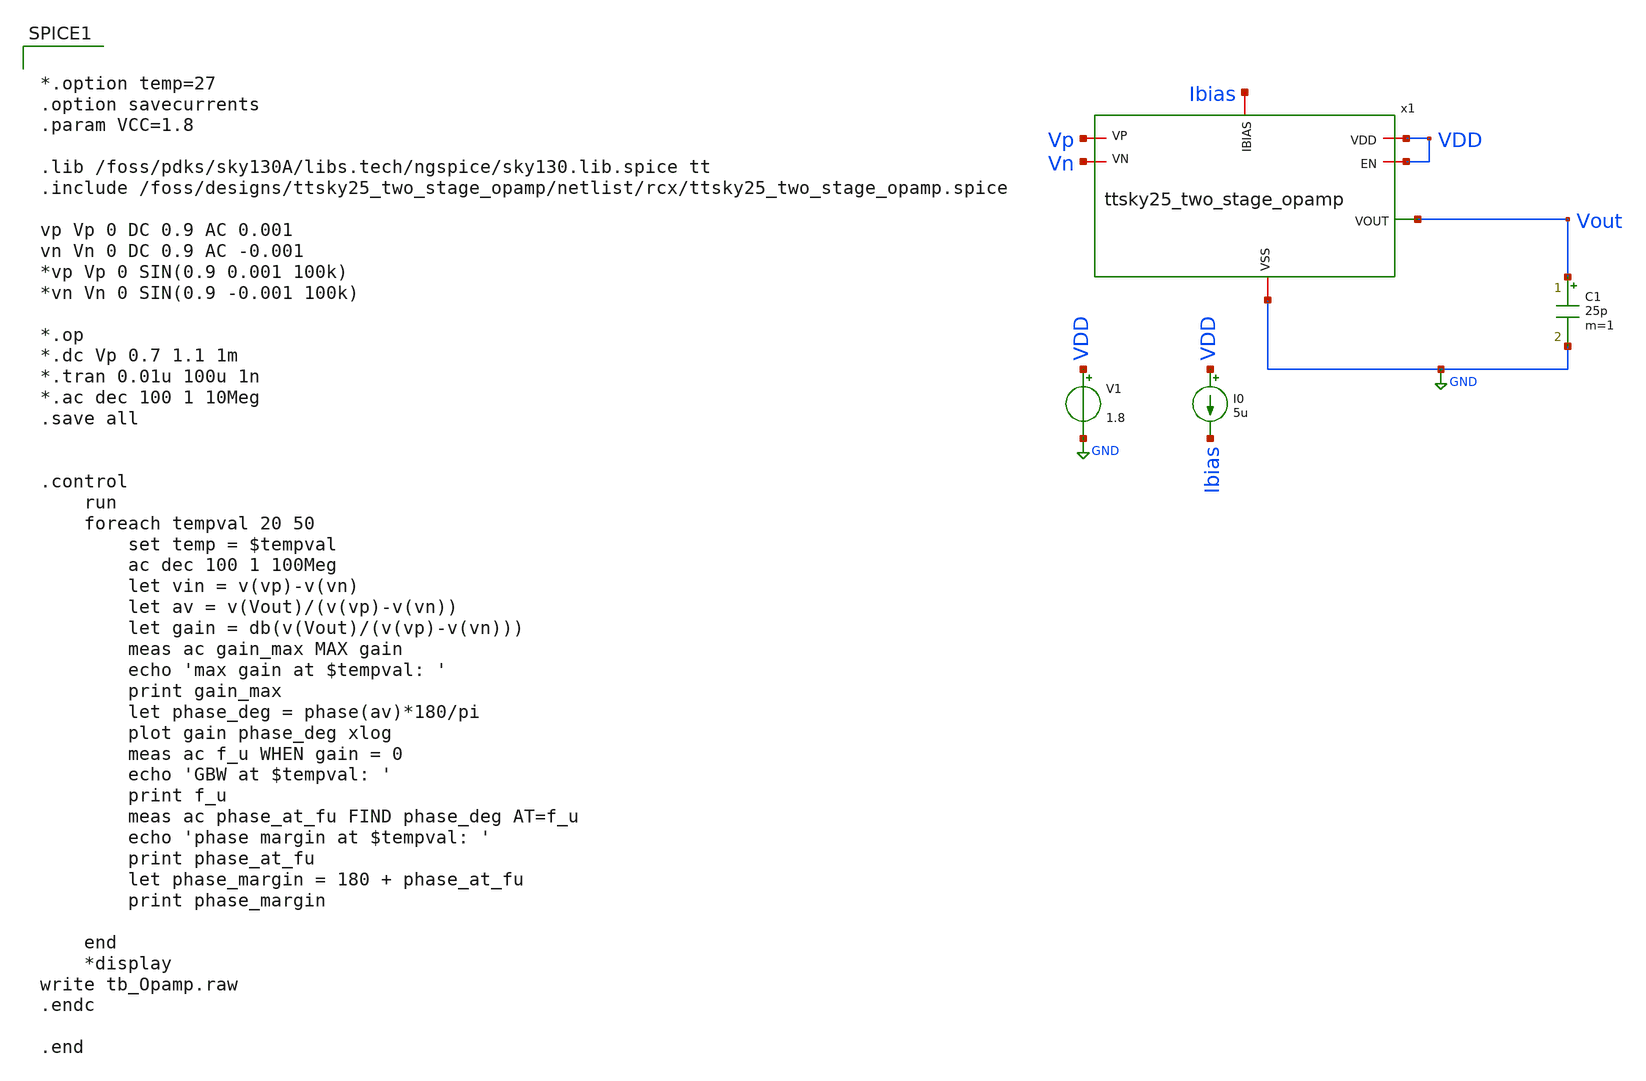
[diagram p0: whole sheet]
** sch_path: xschem/post-layout/testbenches/tb_Opamp.sch
**.subckt tb_Opamp
V1 VDD GND 1.8
C1 Vout GND 25p m=1
I0 VDD Ibias 5u
x1 VDD Ibias Vout Vn Vp VDD GND ttsky25_two_stage_opamp
**** begin user architecture code


*.option temp=27
.option savecurrents
.param VCC=1.8

.lib /foss/pdks/sky130A/libs.tech/ngspice/sky130.lib.spice tt
.include /foss/designs/ttsky25_two_stage_opamp/netlist/rcx/ttsky25_two_stage_opamp.spice

vp Vp 0 DC 0.9 AC 0.001
vn Vn 0 DC 0.9 AC -0.001
*vp Vp 0 SIN(0.9 0.001 100k)
*vn Vn 0 SIN(0.9 -0.001 100k)

*.op
*.dc Vp 0.7 1.1 1m
*.tran 0.01u 100u 1n
*.ac dec 100 1 10Meg
.save all


.control
	run
	foreach tempval 20 50
		set temp = $tempval
		ac dec 100 1 100Meg
		let vin = v(vp)-v(vn)
		let av = v(Vout)/(v(vp)-v(vn))
		let gain = db(v(Vout)/(v(vp)-v(vn)))
		meas ac gain_max MAX gain
		echo 'max gain at $tempval: '
		print gain_max
		let phase_deg = phase(av)*180/pi
		plot gain phase_deg xlog
		meas ac f_u WHEN gain = 0
		echo 'GBW at $tempval: '
		print f_u
		meas ac phase_at_fu FIND phase_deg AT=f_u
		echo 'phase margin at $tempval: '
		print phase_at_fu
		let phase_margin = 180 + phase_at_fu
		print phase_margin

	end
	*display
write tb_Opamp.raw
.endc

.end


**** end user architecture code
**.ends

* expanding   symbol:  ttsky25_two_stage_opamp.sym # of pins=7
** sym_path: xschem/ttsky25_two_stage_opamp.sym
** sch_path: xschem/ttsky25_two_stage_opamp.sch
.subckt ttsky25_two_stage_opamp VDD IBIAS VOUT VN VP EN VSS
*.iopin VSS
*.iopin VDD
*.iopin IBIAS
*.opin VOUT
*.iopin EN
*.iopin VN
*.iopin VP
XC2 net1 VOUT sky130_fd_pr__cap_mim_m3_1 W=25.5 L=25.5 MF=1 m=1
XM5 net2 net2 net2 VSS sky130_fd_pr__nfet_01v8_lvt L=1 W=7 nf=1 ad='int((1 + 1)/2) * 7 / 1 * 0.29' as='int((1 + 2)/2) * 7 / 1 * 0.29'
+ pd='2*int((1 + 1)/2) * (7 / 1 + 0.29)' ps='2*int((1 + 2)/2) * (7 / 1 + 0.29)' nrd='0.29 / 7 ' nrs='0.29 / 7 '
+ sa=0 sb=0 sd=0 mult=1 m=1
XM6 IBIAS EN net2 VSS sky130_fd_pr__nfet_01v8_lvt L=1 W=7 nf=1 ad='int((1 + 1)/2) * 7 / 1 * 0.29' as='int((1 + 2)/2) * 7 / 1 * 0.29'
+ pd='2*int((1 + 1)/2) * (7 / 1 + 0.29)' ps='2*int((1 + 2)/2) * (7 / 1 + 0.29)' nrd='0.29 / 7 ' nrs='0.29 / 7 '
+ sa=0 sb=0 sd=0 mult=1 m=1
XM8 IBIAS IBIAS IBIAS VSS sky130_fd_pr__nfet_01v8_lvt L=1 W=7 nf=1 ad='int((1 + 1)/2) * 7 / 1 * 0.29'
+ as='int((1 + 2)/2) * 7 / 1 * 0.29' pd='2*int((1 + 1)/2) * (7 / 1 + 0.29)' ps='2*int((1 + 2)/2) * (7 / 1 + 0.29)'
+ nrd='0.29 / 7 ' nrs='0.29 / 7 ' sa=0 sb=0 sd=0 mult=1 m=1
XM9 Vz Vz Vz VSS sky130_fd_pr__nfet_01v8_lvt L=1 W=7 nf=1 ad='int((1 + 1)/2) * 7 / 1 * 0.29' as='int((1 + 2)/2) * 7 / 1 * 0.29'
+ pd='2*int((1 + 1)/2) * (7 / 1 + 0.29)' ps='2*int((1 + 2)/2) * (7 / 1 + 0.29)' nrd='0.29 / 7 ' nrs='0.29 / 7 '
+ sa=0 sb=0 sd=0 mult=1 m=1
XM10 Vz EN net3 VSS sky130_fd_pr__nfet_01v8_lvt L=1 W=7 nf=1 ad='int((1 + 1)/2) * 7 / 1 * 0.29' as='int((1 + 2)/2) * 7 / 1 * 0.29'
+ pd='2*int((1 + 1)/2) * (7 / 1 + 0.29)' ps='2*int((1 + 2)/2) * (7 / 1 + 0.29)' nrd='0.29 / 7 ' nrs='0.29 / 7 '
+ sa=0 sb=0 sd=0 mult=1 m=1
XM11 net3 net3 net3 VSS sky130_fd_pr__nfet_01v8_lvt L=1 W=7 nf=1 ad='int((1 + 1)/2) * 7 / 1 * 0.29' as='int((1 + 2)/2) * 7 / 1 * 0.29'
+ pd='2*int((1 + 1)/2) * (7 / 1 + 0.29)' ps='2*int((1 + 2)/2) * (7 / 1 + 0.29)' nrd='0.29 / 7 ' nrs='0.29 / 7 '
+ sa=0 sb=0 sd=0 mult=1 m=1
XM13 VOUT EN net4 VSS sky130_fd_pr__nfet_01v8_lvt L=1 W=7 nf=1 ad='int((1 + 1)/2) * 7 / 1 * 0.29' as='int((1 + 2)/2) * 7 / 1 * 0.29'
+ pd='2*int((1 + 1)/2) * (7 / 1 + 0.29)' ps='2*int((1 + 2)/2) * (7 / 1 + 0.29)' nrd='0.29 / 7 ' nrs='0.29 / 7 '
+ sa=0 sb=0 sd=0 mult=1 m=1
XM14 VOUT VOUT VOUT VSS sky130_fd_pr__nfet_01v8_lvt L=1 W=7 nf=1 ad='int((1 + 1)/2) * 7 / 1 * 0.29' as='int((1 + 2)/2) * 7 / 1 * 0.29'
+ pd='2*int((1 + 1)/2) * (7 / 1 + 0.29)' ps='2*int((1 + 2)/2) * (7 / 1 + 0.29)' nrd='0.29 / 7 ' nrs='0.29 / 7 '
+ sa=0 sb=0 sd=0 mult=1 m=1
XM15 net4 net4 net4 VSS sky130_fd_pr__nfet_01v8_lvt L=1 W=7 nf=1 ad='int((1 + 1)/2) * 7 / 1 * 0.29' as='int((1 + 2)/2) * 7 / 1 * 0.29'
+ pd='2*int((1 + 1)/2) * (7 / 1 + 0.29)' ps='2*int((1 + 2)/2) * (7 / 1 + 0.29)' nrd='0.29 / 7 ' nrs='0.29 / 7 '
+ sa=0 sb=0 sd=0 mult=1 m=1
XM16 net2 net2 VSS VSS sky130_fd_pr__nfet_01v8_lvt L=1 W=3 nf=1 ad='int((1 + 1)/2) * 3 / 1 * 0.29' as='int((1 + 2)/2) * 3 / 1 * 0.29'
+ pd='2*int((1 + 1)/2) * (3 / 1 + 0.29)' ps='2*int((1 + 2)/2) * (3 / 1 + 0.29)' nrd='0.29 / 3 ' nrs='0.29 / 3 '
+ sa=0 sb=0 sd=0 mult=1 m=1
XM17 net2 net2 VSS VSS sky130_fd_pr__nfet_01v8_lvt L=1 W=3 nf=1 ad='int((1 + 1)/2) * 3 / 1 * 0.29' as='int((1 + 2)/2) * 3 / 1 * 0.29'
+ pd='2*int((1 + 1)/2) * (3 / 1 + 0.29)' ps='2*int((1 + 2)/2) * (3 / 1 + 0.29)' nrd='0.29 / 3 ' nrs='0.29 / 3 '
+ sa=0 sb=0 sd=0 mult=1 m=1
XM18 net3 net2 VSS VSS sky130_fd_pr__nfet_01v8_lvt L=1 W=3 nf=1 ad='int((1 + 1)/2) * 3 / 1 * 0.29' as='int((1 + 2)/2) * 3 / 1 * 0.29'
+ pd='2*int((1 + 1)/2) * (3 / 1 + 0.29)' ps='2*int((1 + 2)/2) * (3 / 1 + 0.29)' nrd='0.29 / 3 ' nrs='0.29 / 3 '
+ sa=0 sb=0 sd=0 mult=1 m=1
XM19 net3 net2 VSS VSS sky130_fd_pr__nfet_01v8_lvt L=1 W=3 nf=1 ad='int((1 + 1)/2) * 3 / 1 * 0.29' as='int((1 + 2)/2) * 3 / 1 * 0.29'
+ pd='2*int((1 + 1)/2) * (3 / 1 + 0.29)' ps='2*int((1 + 2)/2) * (3 / 1 + 0.29)' nrd='0.29 / 3 ' nrs='0.29 / 3 '
+ sa=0 sb=0 sd=0 mult=1 m=1
XM20 net3 net2 VSS VSS sky130_fd_pr__nfet_01v8_lvt L=1 W=3 nf=1 ad='int((1 + 1)/2) * 3 / 1 * 0.29' as='int((1 + 2)/2) * 3 / 1 * 0.29'
+ pd='2*int((1 + 1)/2) * (3 / 1 + 0.29)' ps='2*int((1 + 2)/2) * (3 / 1 + 0.29)' nrd='0.29 / 3 ' nrs='0.29 / 3 '
+ sa=0 sb=0 sd=0 mult=1 m=1
XM21 net3 net2 VSS VSS sky130_fd_pr__nfet_01v8_lvt L=1 W=3 nf=1 ad='int((1 + 1)/2) * 3 / 1 * 0.29' as='int((1 + 2)/2) * 3 / 1 * 0.29'
+ pd='2*int((1 + 1)/2) * (3 / 1 + 0.29)' ps='2*int((1 + 2)/2) * (3 / 1 + 0.29)' nrd='0.29 / 3 ' nrs='0.29 / 3 '
+ sa=0 sb=0 sd=0 mult=1 m=1
XM22 net3 net2 VSS VSS sky130_fd_pr__nfet_01v8_lvt L=1 W=3 nf=1 ad='int((1 + 1)/2) * 3 / 1 * 0.29' as='int((1 + 2)/2) * 3 / 1 * 0.29'
+ pd='2*int((1 + 1)/2) * (3 / 1 + 0.29)' ps='2*int((1 + 2)/2) * (3 / 1 + 0.29)' nrd='0.29 / 3 ' nrs='0.29 / 3 '
+ sa=0 sb=0 sd=0 mult=1 m=1
XM23 net3 net2 VSS VSS sky130_fd_pr__nfet_01v8_lvt L=1 W=3 nf=1 ad='int((1 + 1)/2) * 3 / 1 * 0.29' as='int((1 + 2)/2) * 3 / 1 * 0.29'
+ pd='2*int((1 + 1)/2) * (3 / 1 + 0.29)' ps='2*int((1 + 2)/2) * (3 / 1 + 0.29)' nrd='0.29 / 3 ' nrs='0.29 / 3 '
+ sa=0 sb=0 sd=0 mult=1 m=1
XM24 net3 net2 VSS VSS sky130_fd_pr__nfet_01v8_lvt L=1 W=3 nf=1 ad='int((1 + 1)/2) * 3 / 1 * 0.29' as='int((1 + 2)/2) * 3 / 1 * 0.29'
+ pd='2*int((1 + 1)/2) * (3 / 1 + 0.29)' ps='2*int((1 + 2)/2) * (3 / 1 + 0.29)' nrd='0.29 / 3 ' nrs='0.29 / 3 '
+ sa=0 sb=0 sd=0 mult=1 m=1
XM25 net3 net2 VSS VSS sky130_fd_pr__nfet_01v8_lvt L=1 W=3 nf=1 ad='int((1 + 1)/2) * 3 / 1 * 0.29' as='int((1 + 2)/2) * 3 / 1 * 0.29'
+ pd='2*int((1 + 1)/2) * (3 / 1 + 0.29)' ps='2*int((1 + 2)/2) * (3 / 1 + 0.29)' nrd='0.29 / 3 ' nrs='0.29 / 3 '
+ sa=0 sb=0 sd=0 mult=1 m=1
XM26 net3 net2 VSS VSS sky130_fd_pr__nfet_01v8_lvt L=1 W=3 nf=1 ad='int((1 + 1)/2) * 3 / 1 * 0.29' as='int((1 + 2)/2) * 3 / 1 * 0.29'
+ pd='2*int((1 + 1)/2) * (3 / 1 + 0.29)' ps='2*int((1 + 2)/2) * (3 / 1 + 0.29)' nrd='0.29 / 3 ' nrs='0.29 / 3 '
+ sa=0 sb=0 sd=0 mult=1 m=1
XM27 net3 net2 VSS VSS sky130_fd_pr__nfet_01v8_lvt L=1 W=3 nf=1 ad='int((1 + 1)/2) * 3 / 1 * 0.29' as='int((1 + 2)/2) * 3 / 1 * 0.29'
+ pd='2*int((1 + 1)/2) * (3 / 1 + 0.29)' ps='2*int((1 + 2)/2) * (3 / 1 + 0.29)' nrd='0.29 / 3 ' nrs='0.29 / 3 '
+ sa=0 sb=0 sd=0 mult=1 m=1
XM28 net3 net2 VSS VSS sky130_fd_pr__nfet_01v8_lvt L=1 W=3 nf=1 ad='int((1 + 1)/2) * 3 / 1 * 0.29' as='int((1 + 2)/2) * 3 / 1 * 0.29'
+ pd='2*int((1 + 1)/2) * (3 / 1 + 0.29)' ps='2*int((1 + 2)/2) * (3 / 1 + 0.29)' nrd='0.29 / 3 ' nrs='0.29 / 3 '
+ sa=0 sb=0 sd=0 mult=1 m=1
XM29 net3 net2 VSS VSS sky130_fd_pr__nfet_01v8_lvt L=1 W=3 nf=1 ad='int((1 + 1)/2) * 3 / 1 * 0.29' as='int((1 + 2)/2) * 3 / 1 * 0.29'
+ pd='2*int((1 + 1)/2) * (3 / 1 + 0.29)' ps='2*int((1 + 2)/2) * (3 / 1 + 0.29)' nrd='0.29 / 3 ' nrs='0.29 / 3 '
+ sa=0 sb=0 sd=0 mult=1 m=1
XM30 VSS VSS VSS VSS sky130_fd_pr__nfet_01v8_lvt L=1 W=3 nf=1 ad='int((1 + 1)/2) * 3 / 1 * 0.29' as='int((1 + 2)/2) * 3 / 1 * 0.29'
+ pd='2*int((1 + 1)/2) * (3 / 1 + 0.29)' ps='2*int((1 + 2)/2) * (3 / 1 + 0.29)' nrd='0.29 / 3 ' nrs='0.29 / 3 '
+ sa=0 sb=0 sd=0 mult=1 m=1
XM31 VSS VSS VSS VSS sky130_fd_pr__nfet_01v8_lvt L=1 W=3 nf=1 ad='int((1 + 1)/2) * 3 / 1 * 0.29' as='int((1 + 2)/2) * 3 / 1 * 0.29'
+ pd='2*int((1 + 1)/2) * (3 / 1 + 0.29)' ps='2*int((1 + 2)/2) * (3 / 1 + 0.29)' nrd='0.29 / 3 ' nrs='0.29 / 3 '
+ sa=0 sb=0 sd=0 mult=1 m=1
XM32 net4 net2 VSS VSS sky130_fd_pr__nfet_01v8_lvt L=1 W=3 nf=1 ad='int((1 + 1)/2) * 3 / 1 * 0.29' as='int((1 + 2)/2) * 3 / 1 * 0.29'
+ pd='2*int((1 + 1)/2) * (3 / 1 + 0.29)' ps='2*int((1 + 2)/2) * (3 / 1 + 0.29)' nrd='0.29 / 3 ' nrs='0.29 / 3 '
+ sa=0 sb=0 sd=0 mult=1 m=1
XM33 net4 net2 VSS VSS sky130_fd_pr__nfet_01v8_lvt L=1 W=3 nf=1 ad='int((1 + 1)/2) * 3 / 1 * 0.29' as='int((1 + 2)/2) * 3 / 1 * 0.29'
+ pd='2*int((1 + 1)/2) * (3 / 1 + 0.29)' ps='2*int((1 + 2)/2) * (3 / 1 + 0.29)' nrd='0.29 / 3 ' nrs='0.29 / 3 '
+ sa=0 sb=0 sd=0 mult=1 m=1
XM34 net4 net2 VSS VSS sky130_fd_pr__nfet_01v8_lvt L=1 W=3 nf=1 ad='int((1 + 1)/2) * 3 / 1 * 0.29' as='int((1 + 2)/2) * 3 / 1 * 0.29'
+ pd='2*int((1 + 1)/2) * (3 / 1 + 0.29)' ps='2*int((1 + 2)/2) * (3 / 1 + 0.29)' nrd='0.29 / 3 ' nrs='0.29 / 3 '
+ sa=0 sb=0 sd=0 mult=1 m=1
XM35 net4 net2 VSS VSS sky130_fd_pr__nfet_01v8_lvt L=1 W=3 nf=1 ad='int((1 + 1)/2) * 3 / 1 * 0.29' as='int((1 + 2)/2) * 3 / 1 * 0.29'
+ pd='2*int((1 + 1)/2) * (3 / 1 + 0.29)' ps='2*int((1 + 2)/2) * (3 / 1 + 0.29)' nrd='0.29 / 3 ' nrs='0.29 / 3 '
+ sa=0 sb=0 sd=0 mult=1 m=1
XM36 net4 net2 VSS VSS sky130_fd_pr__nfet_01v8_lvt L=1 W=3 nf=1 ad='int((1 + 1)/2) * 3 / 1 * 0.29' as='int((1 + 2)/2) * 3 / 1 * 0.29'
+ pd='2*int((1 + 1)/2) * (3 / 1 + 0.29)' ps='2*int((1 + 2)/2) * (3 / 1 + 0.29)' nrd='0.29 / 3 ' nrs='0.29 / 3 '
+ sa=0 sb=0 sd=0 mult=1 m=1
XM37 net4 net2 VSS VSS sky130_fd_pr__nfet_01v8_lvt L=1 W=3 nf=1 ad='int((1 + 1)/2) * 3 / 1 * 0.29' as='int((1 + 2)/2) * 3 / 1 * 0.29'
+ pd='2*int((1 + 1)/2) * (3 / 1 + 0.29)' ps='2*int((1 + 2)/2) * (3 / 1 + 0.29)' nrd='0.29 / 3 ' nrs='0.29 / 3 '
+ sa=0 sb=0 sd=0 mult=1 m=1
XM38 net4 net2 VSS VSS sky130_fd_pr__nfet_01v8_lvt L=1 W=3 nf=1 ad='int((1 + 1)/2) * 3 / 1 * 0.29' as='int((1 + 2)/2) * 3 / 1 * 0.29'
+ pd='2*int((1 + 1)/2) * (3 / 1 + 0.29)' ps='2*int((1 + 2)/2) * (3 / 1 + 0.29)' nrd='0.29 / 3 ' nrs='0.29 / 3 '
+ sa=0 sb=0 sd=0 mult=1 m=1
XM39 net4 net2 VSS VSS sky130_fd_pr__nfet_01v8_lvt L=1 W=3 nf=1 ad='int((1 + 1)/2) * 3 / 1 * 0.29' as='int((1 + 2)/2) * 3 / 1 * 0.29'
+ pd='2*int((1 + 1)/2) * (3 / 1 + 0.29)' ps='2*int((1 + 2)/2) * (3 / 1 + 0.29)' nrd='0.29 / 3 ' nrs='0.29 / 3 '
+ sa=0 sb=0 sd=0 mult=1 m=1
XM40 net4 net2 VSS VSS sky130_fd_pr__nfet_01v8_lvt L=1 W=3 nf=1 ad='int((1 + 1)/2) * 3 / 1 * 0.29' as='int((1 + 2)/2) * 3 / 1 * 0.29'
+ pd='2*int((1 + 1)/2) * (3 / 1 + 0.29)' ps='2*int((1 + 2)/2) * (3 / 1 + 0.29)' nrd='0.29 / 3 ' nrs='0.29 / 3 '
+ sa=0 sb=0 sd=0 mult=1 m=1
XM41 net4 net2 VSS VSS sky130_fd_pr__nfet_01v8_lvt L=1 W=3 nf=1 ad='int((1 + 1)/2) * 3 / 1 * 0.29' as='int((1 + 2)/2) * 3 / 1 * 0.29'
+ pd='2*int((1 + 1)/2) * (3 / 1 + 0.29)' ps='2*int((1 + 2)/2) * (3 / 1 + 0.29)' nrd='0.29 / 3 ' nrs='0.29 / 3 '
+ sa=0 sb=0 sd=0 mult=1 m=1
XM42 net4 net2 VSS VSS sky130_fd_pr__nfet_01v8_lvt L=1 W=3 nf=1 ad='int((1 + 1)/2) * 3 / 1 * 0.29' as='int((1 + 2)/2) * 3 / 1 * 0.29'
+ pd='2*int((1 + 1)/2) * (3 / 1 + 0.29)' ps='2*int((1 + 2)/2) * (3 / 1 + 0.29)' nrd='0.29 / 3 ' nrs='0.29 / 3 '
+ sa=0 sb=0 sd=0 mult=1 m=1
XM43 net4 net2 VSS VSS sky130_fd_pr__nfet_01v8_lvt L=1 W=3 nf=1 ad='int((1 + 1)/2) * 3 / 1 * 0.29' as='int((1 + 2)/2) * 3 / 1 * 0.29'
+ pd='2*int((1 + 1)/2) * (3 / 1 + 0.29)' ps='2*int((1 + 2)/2) * (3 / 1 + 0.29)' nrd='0.29 / 3 ' nrs='0.29 / 3 '
+ sa=0 sb=0 sd=0 mult=1 m=1
XM44 VSS VSS VSS VSS sky130_fd_pr__nfet_01v8_lvt L=1 W=3 nf=1 ad='int((1 + 1)/2) * 3 / 1 * 0.29' as='int((1 + 2)/2) * 3 / 1 * 0.29'
+ pd='2*int((1 + 1)/2) * (3 / 1 + 0.29)' ps='2*int((1 + 2)/2) * (3 / 1 + 0.29)' nrd='0.29 / 3 ' nrs='0.29 / 3 '
+ sa=0 sb=0 sd=0 mult=1 m=1
XM45 VSS VSS VSS VSS sky130_fd_pr__nfet_01v8_lvt L=1 W=3 nf=1 ad='int((1 + 1)/2) * 3 / 1 * 0.29' as='int((1 + 2)/2) * 3 / 1 * 0.29'
+ pd='2*int((1 + 1)/2) * (3 / 1 + 0.29)' ps='2*int((1 + 2)/2) * (3 / 1 + 0.29)' nrd='0.29 / 3 ' nrs='0.29 / 3 '
+ sa=0 sb=0 sd=0 mult=1 m=1
XM46 VSS VSS VSS VSS sky130_fd_pr__nfet_01v8_lvt L=1 W=3 nf=1 ad='int((1 + 1)/2) * 3 / 1 * 0.29' as='int((1 + 2)/2) * 3 / 1 * 0.29'
+ pd='2*int((1 + 1)/2) * (3 / 1 + 0.29)' ps='2*int((1 + 2)/2) * (3 / 1 + 0.29)' nrd='0.29 / 3 ' nrs='0.29 / 3 '
+ sa=0 sb=0 sd=0 mult=1 m=1
XM47 VSS VSS VSS VSS sky130_fd_pr__nfet_01v8_lvt L=1 W=3 nf=1 ad='int((1 + 1)/2) * 3 / 1 * 0.29' as='int((1 + 2)/2) * 3 / 1 * 0.29'
+ pd='2*int((1 + 1)/2) * (3 / 1 + 0.29)' ps='2*int((1 + 2)/2) * (3 / 1 + 0.29)' nrd='0.29 / 3 ' nrs='0.29 / 3 '
+ sa=0 sb=0 sd=0 mult=1 m=1
XM48 net4 net2 VSS VSS sky130_fd_pr__nfet_01v8_lvt L=1 W=3 nf=1 ad='int((1 + 1)/2) * 3 / 1 * 0.29' as='int((1 + 2)/2) * 3 / 1 * 0.29'
+ pd='2*int((1 + 1)/2) * (3 / 1 + 0.29)' ps='2*int((1 + 2)/2) * (3 / 1 + 0.29)' nrd='0.29 / 3 ' nrs='0.29 / 3 '
+ sa=0 sb=0 sd=0 mult=1 m=1
XM49 net4 net2 VSS VSS sky130_fd_pr__nfet_01v8_lvt L=1 W=3 nf=1 ad='int((1 + 1)/2) * 3 / 1 * 0.29' as='int((1 + 2)/2) * 3 / 1 * 0.29'
+ pd='2*int((1 + 1)/2) * (3 / 1 + 0.29)' ps='2*int((1 + 2)/2) * (3 / 1 + 0.29)' nrd='0.29 / 3 ' nrs='0.29 / 3 '
+ sa=0 sb=0 sd=0 mult=1 m=1
XM50 net4 net2 VSS VSS sky130_fd_pr__nfet_01v8_lvt L=1 W=3 nf=1 ad='int((1 + 1)/2) * 3 / 1 * 0.29' as='int((1 + 2)/2) * 3 / 1 * 0.29'
+ pd='2*int((1 + 1)/2) * (3 / 1 + 0.29)' ps='2*int((1 + 2)/2) * (3 / 1 + 0.29)' nrd='0.29 / 3 ' nrs='0.29 / 3 '
+ sa=0 sb=0 sd=0 mult=1 m=1
XM51 net4 net2 VSS VSS sky130_fd_pr__nfet_01v8_lvt L=1 W=3 nf=1 ad='int((1 + 1)/2) * 3 / 1 * 0.29' as='int((1 + 2)/2) * 3 / 1 * 0.29'
+ pd='2*int((1 + 1)/2) * (3 / 1 + 0.29)' ps='2*int((1 + 2)/2) * (3 / 1 + 0.29)' nrd='0.29 / 3 ' nrs='0.29 / 3 '
+ sa=0 sb=0 sd=0 mult=1 m=1
XM52 net4 net2 VSS VSS sky130_fd_pr__nfet_01v8_lvt L=1 W=3 nf=1 ad='int((1 + 1)/2) * 3 / 1 * 0.29' as='int((1 + 2)/2) * 3 / 1 * 0.29'
+ pd='2*int((1 + 1)/2) * (3 / 1 + 0.29)' ps='2*int((1 + 2)/2) * (3 / 1 + 0.29)' nrd='0.29 / 3 ' nrs='0.29 / 3 '
+ sa=0 sb=0 sd=0 mult=1 m=1
XM53 net4 net2 VSS VSS sky130_fd_pr__nfet_01v8_lvt L=1 W=3 nf=1 ad='int((1 + 1)/2) * 3 / 1 * 0.29' as='int((1 + 2)/2) * 3 / 1 * 0.29'
+ pd='2*int((1 + 1)/2) * (3 / 1 + 0.29)' ps='2*int((1 + 2)/2) * (3 / 1 + 0.29)' nrd='0.29 / 3 ' nrs='0.29 / 3 '
+ sa=0 sb=0 sd=0 mult=1 m=1
XM54 net4 net2 VSS VSS sky130_fd_pr__nfet_01v8_lvt L=1 W=3 nf=1 ad='int((1 + 1)/2) * 3 / 1 * 0.29' as='int((1 + 2)/2) * 3 / 1 * 0.29'
+ pd='2*int((1 + 1)/2) * (3 / 1 + 0.29)' ps='2*int((1 + 2)/2) * (3 / 1 + 0.29)' nrd='0.29 / 3 ' nrs='0.29 / 3 '
+ sa=0 sb=0 sd=0 mult=1 m=1
XM55 net4 net2 VSS VSS sky130_fd_pr__nfet_01v8_lvt L=1 W=3 nf=1 ad='int((1 + 1)/2) * 3 / 1 * 0.29' as='int((1 + 2)/2) * 3 / 1 * 0.29'
+ pd='2*int((1 + 1)/2) * (3 / 1 + 0.29)' ps='2*int((1 + 2)/2) * (3 / 1 + 0.29)' nrd='0.29 / 3 ' nrs='0.29 / 3 '
+ sa=0 sb=0 sd=0 mult=1 m=1
XM56 net4 net2 VSS VSS sky130_fd_pr__nfet_01v8_lvt L=1 W=3 nf=1 ad='int((1 + 1)/2) * 3 / 1 * 0.29' as='int((1 + 2)/2) * 3 / 1 * 0.29'
+ pd='2*int((1 + 1)/2) * (3 / 1 + 0.29)' ps='2*int((1 + 2)/2) * (3 / 1 + 0.29)' nrd='0.29 / 3 ' nrs='0.29 / 3 '
+ sa=0 sb=0 sd=0 mult=1 m=1
XM57 net4 net2 VSS VSS sky130_fd_pr__nfet_01v8_lvt L=1 W=3 nf=1 ad='int((1 + 1)/2) * 3 / 1 * 0.29' as='int((1 + 2)/2) * 3 / 1 * 0.29'
+ pd='2*int((1 + 1)/2) * (3 / 1 + 0.29)' ps='2*int((1 + 2)/2) * (3 / 1 + 0.29)' nrd='0.29 / 3 ' nrs='0.29 / 3 '
+ sa=0 sb=0 sd=0 mult=1 m=1
XM58 net4 net2 VSS VSS sky130_fd_pr__nfet_01v8_lvt L=1 W=3 nf=1 ad='int((1 + 1)/2) * 3 / 1 * 0.29' as='int((1 + 2)/2) * 3 / 1 * 0.29'
+ pd='2*int((1 + 1)/2) * (3 / 1 + 0.29)' ps='2*int((1 + 2)/2) * (3 / 1 + 0.29)' nrd='0.29 / 3 ' nrs='0.29 / 3 '
+ sa=0 sb=0 sd=0 mult=1 m=1
XM59 net4 net2 VSS VSS sky130_fd_pr__nfet_01v8_lvt L=1 W=3 nf=1 ad='int((1 + 1)/2) * 3 / 1 * 0.29' as='int((1 + 2)/2) * 3 / 1 * 0.29'
+ pd='2*int((1 + 1)/2) * (3 / 1 + 0.29)' ps='2*int((1 + 2)/2) * (3 / 1 + 0.29)' nrd='0.29 / 3 ' nrs='0.29 / 3 '
+ sa=0 sb=0 sd=0 mult=1 m=1
XM60 VSS VSS VSS VSS sky130_fd_pr__nfet_01v8_lvt L=1 W=3 nf=1 ad='int((1 + 1)/2) * 3 / 1 * 0.29' as='int((1 + 2)/2) * 3 / 1 * 0.29'
+ pd='2*int((1 + 1)/2) * (3 / 1 + 0.29)' ps='2*int((1 + 2)/2) * (3 / 1 + 0.29)' nrd='0.29 / 3 ' nrs='0.29 / 3 '
+ sa=0 sb=0 sd=0 mult=1 m=1
XM61 VSS VSS VSS VSS sky130_fd_pr__nfet_01v8_lvt L=1 W=3 nf=1 ad='int((1 + 1)/2) * 3 / 1 * 0.29' as='int((1 + 2)/2) * 3 / 1 * 0.29'
+ pd='2*int((1 + 1)/2) * (3 / 1 + 0.29)' ps='2*int((1 + 2)/2) * (3 / 1 + 0.29)' nrd='0.29 / 3 ' nrs='0.29 / 3 '
+ sa=0 sb=0 sd=0 mult=1 m=1
XM62 VSS VSS VSS VSS sky130_fd_pr__nfet_01v8_lvt L=1 W=3 nf=1 ad='int((1 + 1)/2) * 3 / 1 * 0.29' as='int((1 + 2)/2) * 3 / 1 * 0.29'
+ pd='2*int((1 + 1)/2) * (3 / 1 + 0.29)' ps='2*int((1 + 2)/2) * (3 / 1 + 0.29)' nrd='0.29 / 3 ' nrs='0.29 / 3 '
+ sa=0 sb=0 sd=0 mult=1 m=1
XM63 VSS VSS VSS VSS sky130_fd_pr__nfet_01v8_lvt L=1 W=3 nf=1 ad='int((1 + 1)/2) * 3 / 1 * 0.29' as='int((1 + 2)/2) * 3 / 1 * 0.29'
+ pd='2*int((1 + 1)/2) * (3 / 1 + 0.29)' ps='2*int((1 + 2)/2) * (3 / 1 + 0.29)' nrd='0.29 / 3 ' nrs='0.29 / 3 '
+ sa=0 sb=0 sd=0 mult=1 m=1
XM68 Vpo Vpo VDD VDD sky130_fd_pr__pfet_01v8 L=0.4 W=1 nf=1 ad='int((nf+1)/2) * W/nf * 0.29' as='int((nf+2)/2) * W/nf * 0.29'
+ pd='2*int((nf+1)/2) * (W/nf + 0.29)' ps='2*int((nf+2)/2) * (W/nf + 0.29)' nrd='0.29 / W' nrs='0.29 / W'
+ sa=0 sb=0 sd=0 mult=1 m=1
XM69 Vpo Vpo VDD VDD sky130_fd_pr__pfet_01v8 L=0.4 W=1 nf=1 ad='int((nf+1)/2) * W/nf * 0.29' as='int((nf+2)/2) * W/nf * 0.29'
+ pd='2*int((nf+1)/2) * (W/nf + 0.29)' ps='2*int((nf+2)/2) * (W/nf + 0.29)' nrd='0.29 / W' nrs='0.29 / W'
+ sa=0 sb=0 sd=0 mult=1 m=1
XM70 Vpo Vpo VDD VDD sky130_fd_pr__pfet_01v8 L=0.4 W=1 nf=1 ad='int((nf+1)/2) * W/nf * 0.29' as='int((nf+2)/2) * W/nf * 0.29'
+ pd='2*int((nf+1)/2) * (W/nf + 0.29)' ps='2*int((nf+2)/2) * (W/nf + 0.29)' nrd='0.29 / W' nrs='0.29 / W'
+ sa=0 sb=0 sd=0 mult=1 m=1
XM71 Vpo Vpo VDD VDD sky130_fd_pr__pfet_01v8 L=0.4 W=1 nf=1 ad='int((nf+1)/2) * W/nf * 0.29' as='int((nf+2)/2) * W/nf * 0.29'
+ pd='2*int((nf+1)/2) * (W/nf + 0.29)' ps='2*int((nf+2)/2) * (W/nf + 0.29)' nrd='0.29 / W' nrs='0.29 / W'
+ sa=0 sb=0 sd=0 mult=1 m=1
XM72 Vout1 Vpo VDD VDD sky130_fd_pr__pfet_01v8 L=0.4 W=1 nf=1 ad='int((nf+1)/2) * W/nf * 0.29' as='int((nf+2)/2) * W/nf * 0.29'
+ pd='2*int((nf+1)/2) * (W/nf + 0.29)' ps='2*int((nf+2)/2) * (W/nf + 0.29)' nrd='0.29 / W' nrs='0.29 / W'
+ sa=0 sb=0 sd=0 mult=1 m=1
XM73 Vout1 Vpo VDD VDD sky130_fd_pr__pfet_01v8 L=0.4 W=1 nf=1 ad='int((nf+1)/2) * W/nf * 0.29' as='int((nf+2)/2) * W/nf * 0.29'
+ pd='2*int((nf+1)/2) * (W/nf + 0.29)' ps='2*int((nf+2)/2) * (W/nf + 0.29)' nrd='0.29 / W' nrs='0.29 / W'
+ sa=0 sb=0 sd=0 mult=1 m=1
XM74 Vout1 Vpo VDD VDD sky130_fd_pr__pfet_01v8 L=0.4 W=1 nf=1 ad='int((nf+1)/2) * W/nf * 0.29' as='int((nf+2)/2) * W/nf * 0.29'
+ pd='2*int((nf+1)/2) * (W/nf + 0.29)' ps='2*int((nf+2)/2) * (W/nf + 0.29)' nrd='0.29 / W' nrs='0.29 / W'
+ sa=0 sb=0 sd=0 mult=1 m=1
XM75 Vout1 Vpo VDD VDD sky130_fd_pr__pfet_01v8 L=0.4 W=1 nf=1 ad='int((nf+1)/2) * W/nf * 0.29' as='int((nf+2)/2) * W/nf * 0.29'
+ pd='2*int((nf+1)/2) * (W/nf + 0.29)' ps='2*int((nf+2)/2) * (W/nf + 0.29)' nrd='0.29 / W' nrs='0.29 / W'
+ sa=0 sb=0 sd=0 mult=1 m=1
XM76 VOUT Vout1 VDD VDD sky130_fd_pr__pfet_01v8 L=0.4 W=1 nf=1 ad='int((nf+1)/2) * W/nf * 0.29' as='int((nf+2)/2) * W/nf * 0.29'
+ pd='2*int((nf+1)/2) * (W/nf + 0.29)' ps='2*int((nf+2)/2) * (W/nf + 0.29)' nrd='0.29 / W' nrs='0.29 / W'
+ sa=0 sb=0 sd=0 mult=1 m=1
XM78 VOUT Vout1 VDD VDD sky130_fd_pr__pfet_01v8 L=0.4 W=1 nf=1 ad='int((nf+1)/2) * W/nf * 0.29' as='int((nf+2)/2) * W/nf * 0.29'
+ pd='2*int((nf+1)/2) * (W/nf + 0.29)' ps='2*int((nf+2)/2) * (W/nf + 0.29)' nrd='0.29 / W' nrs='0.29 / W'
+ sa=0 sb=0 sd=0 mult=1 m=1
XM79 VOUT Vout1 VDD VDD sky130_fd_pr__pfet_01v8 L=0.4 W=1 nf=1 ad='int((nf+1)/2) * W/nf * 0.29' as='int((nf+2)/2) * W/nf * 0.29'
+ pd='2*int((nf+1)/2) * (W/nf + 0.29)' ps='2*int((nf+2)/2) * (W/nf + 0.29)' nrd='0.29 / W' nrs='0.29 / W'
+ sa=0 sb=0 sd=0 mult=1 m=1
XM80 VOUT Vout1 VDD VDD sky130_fd_pr__pfet_01v8 L=0.4 W=1 nf=1 ad='int((nf+1)/2) * W/nf * 0.29' as='int((nf+2)/2) * W/nf * 0.29'
+ pd='2*int((nf+1)/2) * (W/nf + 0.29)' ps='2*int((nf+2)/2) * (W/nf + 0.29)' nrd='0.29 / W' nrs='0.29 / W'
+ sa=0 sb=0 sd=0 mult=1 m=1
XM81 VOUT Vout1 VDD VDD sky130_fd_pr__pfet_01v8 L=0.4 W=1 nf=1 ad='int((nf+1)/2) * W/nf * 0.29' as='int((nf+2)/2) * W/nf * 0.29'
+ pd='2*int((nf+1)/2) * (W/nf + 0.29)' ps='2*int((nf+2)/2) * (W/nf + 0.29)' nrd='0.29 / W' nrs='0.29 / W'
+ sa=0 sb=0 sd=0 mult=1 m=1
XM82 VOUT Vout1 VDD VDD sky130_fd_pr__pfet_01v8 L=0.4 W=1 nf=1 ad='int((nf+1)/2) * W/nf * 0.29' as='int((nf+2)/2) * W/nf * 0.29'
+ pd='2*int((nf+1)/2) * (W/nf + 0.29)' ps='2*int((nf+2)/2) * (W/nf + 0.29)' nrd='0.29 / W' nrs='0.29 / W'
+ sa=0 sb=0 sd=0 mult=1 m=1
XM83 VOUT Vout1 VDD VDD sky130_fd_pr__pfet_01v8 L=0.4 W=1 nf=1 ad='int((nf+1)/2) * W/nf * 0.29' as='int((nf+2)/2) * W/nf * 0.29'
+ pd='2*int((nf+1)/2) * (W/nf + 0.29)' ps='2*int((nf+2)/2) * (W/nf + 0.29)' nrd='0.29 / W' nrs='0.29 / W'
+ sa=0 sb=0 sd=0 mult=1 m=1
XM84 VOUT Vout1 VDD VDD sky130_fd_pr__pfet_01v8 L=0.4 W=1 nf=1 ad='int((nf+1)/2) * W/nf * 0.29' as='int((nf+2)/2) * W/nf * 0.29'
+ pd='2*int((nf+1)/2) * (W/nf + 0.29)' ps='2*int((nf+2)/2) * (W/nf + 0.29)' nrd='0.29 / W' nrs='0.29 / W'
+ sa=0 sb=0 sd=0 mult=1 m=1
XM87 VOUT Vout1 VDD VDD sky130_fd_pr__pfet_01v8 L=0.4 W=1 nf=1 ad='int((nf+1)/2) * W/nf * 0.29' as='int((nf+2)/2) * W/nf * 0.29'
+ pd='2*int((nf+1)/2) * (W/nf + 0.29)' ps='2*int((nf+2)/2) * (W/nf + 0.29)' nrd='0.29 / W' nrs='0.29 / W'
+ sa=0 sb=0 sd=0 mult=1 m=1
XM88 VOUT Vout1 VDD VDD sky130_fd_pr__pfet_01v8 L=0.4 W=1 nf=1 ad='int((nf+1)/2) * W/nf * 0.29' as='int((nf+2)/2) * W/nf * 0.29'
+ pd='2*int((nf+1)/2) * (W/nf + 0.29)' ps='2*int((nf+2)/2) * (W/nf + 0.29)' nrd='0.29 / W' nrs='0.29 / W'
+ sa=0 sb=0 sd=0 mult=1 m=1
XM91 VOUT Vout1 VDD VDD sky130_fd_pr__pfet_01v8 L=0.4 W=1 nf=1 ad='int((nf+1)/2) * W/nf * 0.29' as='int((nf+2)/2) * W/nf * 0.29'
+ pd='2*int((nf+1)/2) * (W/nf + 0.29)' ps='2*int((nf+2)/2) * (W/nf + 0.29)' nrd='0.29 / W' nrs='0.29 / W'
+ sa=0 sb=0 sd=0 mult=1 m=1
XM92 VOUT Vout1 VDD VDD sky130_fd_pr__pfet_01v8 L=0.4 W=1 nf=1 ad='int((nf+1)/2) * W/nf * 0.29' as='int((nf+2)/2) * W/nf * 0.29'
+ pd='2*int((nf+1)/2) * (W/nf + 0.29)' ps='2*int((nf+2)/2) * (W/nf + 0.29)' nrd='0.29 / W' nrs='0.29 / W'
+ sa=0 sb=0 sd=0 mult=1 m=1
XM97 VOUT VOUT VOUT VDD sky130_fd_pr__pfet_01v8 L=0.4 W=1 nf=1 ad='int((nf+1)/2) * W/nf * 0.29' as='int((nf+2)/2) * W/nf * 0.29'
+ pd='2*int((nf+1)/2) * (W/nf + 0.29)' ps='2*int((nf+2)/2) * (W/nf + 0.29)' nrd='0.29 / W' nrs='0.29 / W'
+ sa=0 sb=0 sd=0 mult=1 m=1
XM98 VDD VDD VDD VDD sky130_fd_pr__pfet_01v8 L=0.4 W=1 nf=1 ad='int((nf+1)/2) * W/nf * 0.29' as='int((nf+2)/2) * W/nf * 0.29'
+ pd='2*int((nf+1)/2) * (W/nf + 0.29)' ps='2*int((nf+2)/2) * (W/nf + 0.29)' nrd='0.29 / W' nrs='0.29 / W'
+ sa=0 sb=0 sd=0 mult=1 m=1
XM99 VOUT Vout1 VDD VDD sky130_fd_pr__pfet_01v8 L=0.4 W=1 nf=1 ad='int((nf+1)/2) * W/nf * 0.29' as='int((nf+2)/2) * W/nf * 0.29'
+ pd='2*int((nf+1)/2) * (W/nf + 0.29)' ps='2*int((nf+2)/2) * (W/nf + 0.29)' nrd='0.29 / W' nrs='0.29 / W'
+ sa=0 sb=0 sd=0 mult=1 m=1
XM100 VOUT VOUT VOUT VDD sky130_fd_pr__pfet_01v8 L=0.4 W=1 nf=1 ad='int((nf+1)/2) * W/nf * 0.29' as='int((nf+2)/2) * W/nf * 0.29'
+ pd='2*int((nf+1)/2) * (W/nf + 0.29)' ps='2*int((nf+2)/2) * (W/nf + 0.29)' nrd='0.29 / W' nrs='0.29 / W'
+ sa=0 sb=0 sd=0 mult=1 m=1
XM3 VDD VDD VDD VDD sky130_fd_pr__pfet_01v8 L=0.4 W=1 nf=1 ad='int((nf+1)/2) * W/nf * 0.29' as='int((nf+2)/2) * W/nf * 0.29'
+ pd='2*int((nf+1)/2) * (W/nf + 0.29)' ps='2*int((nf+2)/2) * (W/nf + 0.29)' nrd='0.29 / W' nrs='0.29 / W'
+ sa=0 sb=0 sd=0 mult=1 m=1
XM4 VOUT Vout1 VDD VDD sky130_fd_pr__pfet_01v8 L=0.4 W=1 nf=1 ad='int((nf+1)/2) * W/nf * 0.29' as='int((nf+2)/2) * W/nf * 0.29'
+ pd='2*int((nf+1)/2) * (W/nf + 0.29)' ps='2*int((nf+2)/2) * (W/nf + 0.29)' nrd='0.29 / W' nrs='0.29 / W'
+ sa=0 sb=0 sd=0 mult=1 m=1
XM7 VOUT Vout1 VDD VDD sky130_fd_pr__pfet_01v8 L=0.4 W=1 nf=1 ad='int((nf+1)/2) * W/nf * 0.29' as='int((nf+2)/2) * W/nf * 0.29'
+ pd='2*int((nf+1)/2) * (W/nf + 0.29)' ps='2*int((nf+2)/2) * (W/nf + 0.29)' nrd='0.29 / W' nrs='0.29 / W'
+ sa=0 sb=0 sd=0 mult=1 m=1
XM12 VOUT Vout1 VDD VDD sky130_fd_pr__pfet_01v8 L=0.4 W=1 nf=1 ad='int((nf+1)/2) * W/nf * 0.29' as='int((nf+2)/2) * W/nf * 0.29'
+ pd='2*int((nf+1)/2) * (W/nf + 0.29)' ps='2*int((nf+2)/2) * (W/nf + 0.29)' nrd='0.29 / W' nrs='0.29 / W'
+ sa=0 sb=0 sd=0 mult=1 m=1
XM64 VOUT VOUT VOUT VDD sky130_fd_pr__pfet_01v8 L=0.4 W=1 nf=1 ad='int((nf+1)/2) * W/nf * 0.29' as='int((nf+2)/2) * W/nf * 0.29'
+ pd='2*int((nf+1)/2) * (W/nf + 0.29)' ps='2*int((nf+2)/2) * (W/nf + 0.29)' nrd='0.29 / W' nrs='0.29 / W'
+ sa=0 sb=0 sd=0 mult=1 m=1
XM65 VDD VDD VDD VDD sky130_fd_pr__pfet_01v8 L=0.4 W=1 nf=1 ad='int((nf+1)/2) * W/nf * 0.29' as='int((nf+2)/2) * W/nf * 0.29'
+ pd='2*int((nf+1)/2) * (W/nf + 0.29)' ps='2*int((nf+2)/2) * (W/nf + 0.29)' nrd='0.29 / W' nrs='0.29 / W'
+ sa=0 sb=0 sd=0 mult=1 m=1
XM66 VDD VDD VDD VDD sky130_fd_pr__pfet_01v8 L=0.4 W=1 nf=1 ad='int((nf+1)/2) * W/nf * 0.29' as='int((nf+2)/2) * W/nf * 0.29'
+ pd='2*int((nf+1)/2) * (W/nf + 0.29)' ps='2*int((nf+2)/2) * (W/nf + 0.29)' nrd='0.29 / W' nrs='0.29 / W'
+ sa=0 sb=0 sd=0 mult=1 m=1
XM67 VDD VDD VDD VDD sky130_fd_pr__pfet_01v8 L=0.4 W=1 nf=1 ad='int((nf+1)/2) * W/nf * 0.29' as='int((nf+2)/2) * W/nf * 0.29'
+ pd='2*int((nf+1)/2) * (W/nf + 0.29)' ps='2*int((nf+2)/2) * (W/nf + 0.29)' nrd='0.29 / W' nrs='0.29 / W'
+ sa=0 sb=0 sd=0 mult=1 m=1
XM77 VDD VDD VDD VDD sky130_fd_pr__pfet_01v8 L=0.4 W=1 nf=1 ad='int((nf+1)/2) * W/nf * 0.29' as='int((nf+2)/2) * W/nf * 0.29'
+ pd='2*int((nf+1)/2) * (W/nf + 0.29)' ps='2*int((nf+2)/2) * (W/nf + 0.29)' nrd='0.29 / W' nrs='0.29 / W'
+ sa=0 sb=0 sd=0 mult=1 m=1
XM85 VDD VDD VDD VDD sky130_fd_pr__pfet_01v8 L=0.4 W=1 nf=1 ad='int((nf+1)/2) * W/nf * 0.29' as='int((nf+2)/2) * W/nf * 0.29'
+ pd='2*int((nf+1)/2) * (W/nf + 0.29)' ps='2*int((nf+2)/2) * (W/nf + 0.29)' nrd='0.29 / W' nrs='0.29 / W'
+ sa=0 sb=0 sd=0 mult=1 m=1
XM86 VDD VDD VDD VDD sky130_fd_pr__pfet_01v8 L=0.4 W=1 nf=1 ad='int((nf+1)/2) * W/nf * 0.29' as='int((nf+2)/2) * W/nf * 0.29'
+ pd='2*int((nf+1)/2) * (W/nf + 0.29)' ps='2*int((nf+2)/2) * (W/nf + 0.29)' nrd='0.29 / W' nrs='0.29 / W'
+ sa=0 sb=0 sd=0 mult=1 m=1
XM89 VDD VDD VDD VDD sky130_fd_pr__pfet_01v8 L=0.4 W=1 nf=1 ad='int((nf+1)/2) * W/nf * 0.29' as='int((nf+2)/2) * W/nf * 0.29'
+ pd='2*int((nf+1)/2) * (W/nf + 0.29)' ps='2*int((nf+2)/2) * (W/nf + 0.29)' nrd='0.29 / W' nrs='0.29 / W'
+ sa=0 sb=0 sd=0 mult=1 m=1
XM90 VDD VDD VDD VDD sky130_fd_pr__pfet_01v8 L=0.4 W=1 nf=1 ad='int((nf+1)/2) * W/nf * 0.29' as='int((nf+2)/2) * W/nf * 0.29'
+ pd='2*int((nf+1)/2) * (W/nf + 0.29)' ps='2*int((nf+2)/2) * (W/nf + 0.29)' nrd='0.29 / W' nrs='0.29 / W'
+ sa=0 sb=0 sd=0 mult=1 m=1
XM93 VDD VDD VDD VDD sky130_fd_pr__pfet_01v8 L=0.4 W=1 nf=1 ad='int((nf+1)/2) * W/nf * 0.29' as='int((nf+2)/2) * W/nf * 0.29'
+ pd='2*int((nf+1)/2) * (W/nf + 0.29)' ps='2*int((nf+2)/2) * (W/nf + 0.29)' nrd='0.29 / W' nrs='0.29 / W'
+ sa=0 sb=0 sd=0 mult=1 m=1
XM94 VDD VDD VDD VDD sky130_fd_pr__pfet_01v8 L=0.4 W=1 nf=1 ad='int((nf+1)/2) * W/nf * 0.29' as='int((nf+2)/2) * W/nf * 0.29'
+ pd='2*int((nf+1)/2) * (W/nf + 0.29)' ps='2*int((nf+2)/2) * (W/nf + 0.29)' nrd='0.29 / W' nrs='0.29 / W'
+ sa=0 sb=0 sd=0 mult=1 m=1
XM95 VDD VDD VDD VDD sky130_fd_pr__pfet_01v8 L=0.4 W=1 nf=1 ad='int((nf+1)/2) * W/nf * 0.29' as='int((nf+2)/2) * W/nf * 0.29'
+ pd='2*int((nf+1)/2) * (W/nf + 0.29)' ps='2*int((nf+2)/2) * (W/nf + 0.29)' nrd='0.29 / W' nrs='0.29 / W'
+ sa=0 sb=0 sd=0 mult=1 m=1
XM96 VDD VDD VDD VDD sky130_fd_pr__pfet_01v8 L=0.4 W=1 nf=1 ad='int((nf+1)/2) * W/nf * 0.29' as='int((nf+2)/2) * W/nf * 0.29'
+ pd='2*int((nf+1)/2) * (W/nf + 0.29)' ps='2*int((nf+2)/2) * (W/nf + 0.29)' nrd='0.29 / W' nrs='0.29 / W'
+ sa=0 sb=0 sd=0 mult=1 m=1
XM101 VDD VDD VDD VDD sky130_fd_pr__pfet_01v8 L=0.4 W=1 nf=1 ad='int((nf+1)/2) * W/nf * 0.29' as='int((nf+2)/2) * W/nf * 0.29'
+ pd='2*int((nf+1)/2) * (W/nf + 0.29)' ps='2*int((nf+2)/2) * (W/nf + 0.29)' nrd='0.29 / W' nrs='0.29 / W'
+ sa=0 sb=0 sd=0 mult=1 m=1
XM102 VDD VDD VDD VDD sky130_fd_pr__pfet_01v8 L=0.4 W=1 nf=1 ad='int((nf+1)/2) * W/nf * 0.29' as='int((nf+2)/2) * W/nf * 0.29'
+ pd='2*int((nf+1)/2) * (W/nf + 0.29)' ps='2*int((nf+2)/2) * (W/nf + 0.29)' nrd='0.29 / W' nrs='0.29 / W'
+ sa=0 sb=0 sd=0 mult=1 m=1
XM103 VDD VDD VDD VDD sky130_fd_pr__pfet_01v8 L=0.4 W=1 nf=1 ad='int((nf+1)/2) * W/nf * 0.29' as='int((nf+2)/2) * W/nf * 0.29'
+ pd='2*int((nf+1)/2) * (W/nf + 0.29)' ps='2*int((nf+2)/2) * (W/nf + 0.29)' nrd='0.29 / W' nrs='0.29 / W'
+ sa=0 sb=0 sd=0 mult=1 m=1
XM104 VDD VDD VDD VDD sky130_fd_pr__pfet_01v8 L=0.4 W=1 nf=1 ad='int((nf+1)/2) * W/nf * 0.29' as='int((nf+2)/2) * W/nf * 0.29'
+ pd='2*int((nf+1)/2) * (W/nf + 0.29)' ps='2*int((nf+2)/2) * (W/nf + 0.29)' nrd='0.29 / W' nrs='0.29 / W'
+ sa=0 sb=0 sd=0 mult=1 m=1
XM105 VOUT Vout1 VDD VDD sky130_fd_pr__pfet_01v8 L=0.4 W=1 nf=1 ad='int((nf+1)/2) * W/nf * 0.29' as='int((nf+2)/2) * W/nf * 0.29'
+ pd='2*int((nf+1)/2) * (W/nf + 0.29)' ps='2*int((nf+2)/2) * (W/nf + 0.29)' nrd='0.29 / W' nrs='0.29 / W'
+ sa=0 sb=0 sd=0 mult=1 m=1
XM106 VOUT VOUT VOUT VDD sky130_fd_pr__pfet_01v8 L=0.4 W=1 nf=1 ad='int((nf+1)/2) * W/nf * 0.29' as='int((nf+2)/2) * W/nf * 0.29'
+ pd='2*int((nf+1)/2) * (W/nf + 0.29)' ps='2*int((nf+2)/2) * (W/nf + 0.29)' nrd='0.29 / W' nrs='0.29 / W'
+ sa=0 sb=0 sd=0 mult=1 m=1
XM107 VOUT Vout1 VDD VDD sky130_fd_pr__pfet_01v8 L=0.4 W=1 nf=1 ad='int((nf+1)/2) * W/nf * 0.29' as='int((nf+2)/2) * W/nf * 0.29'
+ pd='2*int((nf+1)/2) * (W/nf + 0.29)' ps='2*int((nf+2)/2) * (W/nf + 0.29)' nrd='0.29 / W' nrs='0.29 / W'
+ sa=0 sb=0 sd=0 mult=1 m=1
XM1 Vpo VN Vz VSS sky130_fd_pr__nfet_01v8_lvt L=1 W=7 nf=1 ad='int((1 + 1)/2) * 7 / 1 * 0.29' as='int((1 + 2)/2) * 7 / 1 * 0.29'
+ pd='2*int((1 + 1)/2) * (7 / 1 + 0.29)' ps='2*int((1 + 2)/2) * (7 / 1 + 0.29)' nrd='0.29 / 7 ' nrs='0.29 / 7 '
+ sa=0 sb=0 sd=0 mult=1 m=1
XM2 Vout1 VP Vz VSS sky130_fd_pr__nfet_01v8_lvt L=1 W=7 nf=1 ad='int((1 + 1)/2) * 7 / 1 * 0.29' as='int((1 + 2)/2) * 7 / 1 * 0.29'
+ pd='2*int((1 + 1)/2) * (7 / 1 + 0.29)' ps='2*int((1 + 2)/2) * (7 / 1 + 0.29)' nrd='0.29 / 7 ' nrs='0.29 / 7 '
+ sa=0 sb=0 sd=0 mult=1 m=1
XM108 Vout1 VP Vz VSS sky130_fd_pr__nfet_01v8_lvt L=1 W=7 nf=1 ad='int((1 + 1)/2) * 7 / 1 * 0.29' as='int((1 + 2)/2) * 7 / 1 * 0.29'
+ pd='2*int((1 + 1)/2) * (7 / 1 + 0.29)' ps='2*int((1 + 2)/2) * (7 / 1 + 0.29)' nrd='0.29 / 7 ' nrs='0.29 / 7 '
+ sa=0 sb=0 sd=0 mult=1 m=1
XM109 Vpo VN Vz VSS sky130_fd_pr__nfet_01v8_lvt L=1 W=7 nf=1 ad='int((1 + 1)/2) * 7 / 1 * 0.29' as='int((1 + 2)/2) * 7 / 1 * 0.29'
+ pd='2*int((1 + 1)/2) * (7 / 1 + 0.29)' ps='2*int((1 + 2)/2) * (7 / 1 + 0.29)' nrd='0.29 / 7 ' nrs='0.29 / 7 '
+ sa=0 sb=0 sd=0 mult=1 m=1
XM110 Vpo VN Vz VSS sky130_fd_pr__nfet_01v8_lvt L=1 W=7 nf=1 ad='int((1 + 1)/2) * 7 / 1 * 0.29' as='int((1 + 2)/2) * 7 / 1 * 0.29'
+ pd='2*int((1 + 1)/2) * (7 / 1 + 0.29)' ps='2*int((1 + 2)/2) * (7 / 1 + 0.29)' nrd='0.29 / 7 ' nrs='0.29 / 7 '
+ sa=0 sb=0 sd=0 mult=1 m=1
XM111 Vout1 VP Vz VSS sky130_fd_pr__nfet_01v8_lvt L=1 W=7 nf=1 ad='int((1 + 1)/2) * 7 / 1 * 0.29' as='int((1 + 2)/2) * 7 / 1 * 0.29'
+ pd='2*int((1 + 1)/2) * (7 / 1 + 0.29)' ps='2*int((1 + 2)/2) * (7 / 1 + 0.29)' nrd='0.29 / 7 ' nrs='0.29 / 7 '
+ sa=0 sb=0 sd=0 mult=1 m=1
XM112 Vout1 VP Vz VSS sky130_fd_pr__nfet_01v8_lvt L=1 W=7 nf=1 ad='int((1 + 1)/2) * 7 / 1 * 0.29' as='int((1 + 2)/2) * 7 / 1 * 0.29'
+ pd='2*int((1 + 1)/2) * (7 / 1 + 0.29)' ps='2*int((1 + 2)/2) * (7 / 1 + 0.29)' nrd='0.29 / 7 ' nrs='0.29 / 7 '
+ sa=0 sb=0 sd=0 mult=1 m=1
XM113 Vpo VN Vz VSS sky130_fd_pr__nfet_01v8_lvt L=1 W=7 nf=1 ad='int((1 + 1)/2) * 7 / 1 * 0.29' as='int((1 + 2)/2) * 7 / 1 * 0.29'
+ pd='2*int((1 + 1)/2) * (7 / 1 + 0.29)' ps='2*int((1 + 2)/2) * (7 / 1 + 0.29)' nrd='0.29 / 7 ' nrs='0.29 / 7 '
+ sa=0 sb=0 sd=0 mult=1 m=1
XM114 Vout1 VP Vz VSS sky130_fd_pr__nfet_01v8_lvt L=1 W=7 nf=1 ad='int((1 + 1)/2) * 7 / 1 * 0.29' as='int((1 + 2)/2) * 7 / 1 * 0.29'
+ pd='2*int((1 + 1)/2) * (7 / 1 + 0.29)' ps='2*int((1 + 2)/2) * (7 / 1 + 0.29)' nrd='0.29 / 7 ' nrs='0.29 / 7 '
+ sa=0 sb=0 sd=0 mult=1 m=1
XM115 Vpo VN Vz VSS sky130_fd_pr__nfet_01v8_lvt L=1 W=7 nf=1 ad='int((1 + 1)/2) * 7 / 1 * 0.29' as='int((1 + 2)/2) * 7 / 1 * 0.29'
+ pd='2*int((1 + 1)/2) * (7 / 1 + 0.29)' ps='2*int((1 + 2)/2) * (7 / 1 + 0.29)' nrd='0.29 / 7 ' nrs='0.29 / 7 '
+ sa=0 sb=0 sd=0 mult=1 m=1
XM116 Vpo VN Vz VSS sky130_fd_pr__nfet_01v8_lvt L=1 W=7 nf=1 ad='int((1 + 1)/2) * 7 / 1 * 0.29' as='int((1 + 2)/2) * 7 / 1 * 0.29'
+ pd='2*int((1 + 1)/2) * (7 / 1 + 0.29)' ps='2*int((1 + 2)/2) * (7 / 1 + 0.29)' nrd='0.29 / 7 ' nrs='0.29 / 7 '
+ sa=0 sb=0 sd=0 mult=1 m=1
XM117 Vout1 VP Vz VSS sky130_fd_pr__nfet_01v8_lvt L=1 W=7 nf=1 ad='int((1 + 1)/2) * 7 / 1 * 0.29' as='int((1 + 2)/2) * 7 / 1 * 0.29'
+ pd='2*int((1 + 1)/2) * (7 / 1 + 0.29)' ps='2*int((1 + 2)/2) * (7 / 1 + 0.29)' nrd='0.29 / 7 ' nrs='0.29 / 7 '
+ sa=0 sb=0 sd=0 mult=1 m=1
XM118 Vout1 VP Vz VSS sky130_fd_pr__nfet_01v8_lvt L=1 W=7 nf=1 ad='int((1 + 1)/2) * 7 / 1 * 0.29' as='int((1 + 2)/2) * 7 / 1 * 0.29'
+ pd='2*int((1 + 1)/2) * (7 / 1 + 0.29)' ps='2*int((1 + 2)/2) * (7 / 1 + 0.29)' nrd='0.29 / 7 ' nrs='0.29 / 7 '
+ sa=0 sb=0 sd=0 mult=1 m=1
XM119 Vpo VN Vz VSS sky130_fd_pr__nfet_01v8_lvt L=1 W=7 nf=1 ad='int((1 + 1)/2) * 7 / 1 * 0.29' as='int((1 + 2)/2) * 7 / 1 * 0.29'
+ pd='2*int((1 + 1)/2) * (7 / 1 + 0.29)' ps='2*int((1 + 2)/2) * (7 / 1 + 0.29)' nrd='0.29 / 7 ' nrs='0.29 / 7 '
+ sa=0 sb=0 sd=0 mult=1 m=1
XM120 Vpo VN Vz VSS sky130_fd_pr__nfet_01v8_lvt L=1 W=7 nf=1 ad='int((1 + 1)/2) * 7 / 1 * 0.29' as='int((1 + 2)/2) * 7 / 1 * 0.29'
+ pd='2*int((1 + 1)/2) * (7 / 1 + 0.29)' ps='2*int((1 + 2)/2) * (7 / 1 + 0.29)' nrd='0.29 / 7 ' nrs='0.29 / 7 '
+ sa=0 sb=0 sd=0 mult=1 m=1
XM121 Vout1 VP Vz VSS sky130_fd_pr__nfet_01v8_lvt L=1 W=7 nf=1 ad='int((1 + 1)/2) * 7 / 1 * 0.29' as='int((1 + 2)/2) * 7 / 1 * 0.29'
+ pd='2*int((1 + 1)/2) * (7 / 1 + 0.29)' ps='2*int((1 + 2)/2) * (7 / 1 + 0.29)' nrd='0.29 / 7 ' nrs='0.29 / 7 '
+ sa=0 sb=0 sd=0 mult=1 m=1
XM122 Vpo Vpo Vpo VSS sky130_fd_pr__nfet_01v8_lvt L=1 W=7 nf=1 ad='int((1 + 1)/2) * 7 / 1 * 0.29' as='int((1 + 2)/2) * 7 / 1 * 0.29'
+ pd='2*int((1 + 1)/2) * (7 / 1 + 0.29)' ps='2*int((1 + 2)/2) * (7 / 1 + 0.29)' nrd='0.29 / 7 ' nrs='0.29 / 7 '
+ sa=0 sb=0 sd=0 mult=1 m=1
XM123 Vpo Vpo Vpo VSS sky130_fd_pr__nfet_01v8_lvt L=1 W=7 nf=1 ad='int((1 + 1)/2) * 7 / 1 * 0.29' as='int((1 + 2)/2) * 7 / 1 * 0.29'
+ pd='2*int((1 + 1)/2) * (7 / 1 + 0.29)' ps='2*int((1 + 2)/2) * (7 / 1 + 0.29)' nrd='0.29 / 7 ' nrs='0.29 / 7 '
+ sa=0 sb=0 sd=0 mult=1 m=1
XM124 Vout1 Vout1 Vout1 VSS sky130_fd_pr__nfet_01v8_lvt L=1 W=7 nf=1 ad='int((1 + 1)/2) * 7 / 1 * 0.29'
+ as='int((1 + 2)/2) * 7 / 1 * 0.29' pd='2*int((1 + 1)/2) * (7 / 1 + 0.29)' ps='2*int((1 + 2)/2) * (7 / 1 + 0.29)'
+ nrd='0.29 / 7 ' nrs='0.29 / 7 ' sa=0 sb=0 sd=0 mult=1 m=1
XM125 Vout1 Vout1 Vout1 VSS sky130_fd_pr__nfet_01v8_lvt L=1 W=7 nf=1 ad='int((1 + 1)/2) * 7 / 1 * 0.29'
+ as='int((1 + 2)/2) * 7 / 1 * 0.29' pd='2*int((1 + 1)/2) * (7 / 1 + 0.29)' ps='2*int((1 + 2)/2) * (7 / 1 + 0.29)'
+ nrd='0.29 / 7 ' nrs='0.29 / 7 ' sa=0 sb=0 sd=0 mult=1 m=1
XM126 VSS VSS VSS VSS sky130_fd_pr__nfet_01v8_lvt L=1 W=7 nf=1 ad='int((1 + 1)/2) * 7 / 1 * 0.29' as='int((1 + 2)/2) * 7 / 1 * 0.29'
+ pd='2*int((1 + 1)/2) * (7 / 1 + 0.29)' ps='2*int((1 + 2)/2) * (7 / 1 + 0.29)' nrd='0.29 / 7 ' nrs='0.29 / 7 '
+ sa=0 sb=0 sd=0 mult=1 m=1
XM127 VSS VSS VSS VSS sky130_fd_pr__nfet_01v8_lvt L=1 W=7 nf=1 ad='int((1 + 1)/2) * 7 / 1 * 0.29' as='int((1 + 2)/2) * 7 / 1 * 0.29'
+ pd='2*int((1 + 1)/2) * (7 / 1 + 0.29)' ps='2*int((1 + 2)/2) * (7 / 1 + 0.29)' nrd='0.29 / 7 ' nrs='0.29 / 7 '
+ sa=0 sb=0 sd=0 mult=1 m=1
XM128 VSS VSS VSS VSS sky130_fd_pr__nfet_01v8_lvt L=1 W=7 nf=1 ad='int((1 + 1)/2) * 7 / 1 * 0.29' as='int((1 + 2)/2) * 7 / 1 * 0.29'
+ pd='2*int((1 + 1)/2) * (7 / 1 + 0.29)' ps='2*int((1 + 2)/2) * (7 / 1 + 0.29)' nrd='0.29 / 7 ' nrs='0.29 / 7 '
+ sa=0 sb=0 sd=0 mult=1 m=1
XM129 VSS VSS VSS VSS sky130_fd_pr__nfet_01v8_lvt L=1 W=7 nf=1 ad='int((1 + 1)/2) * 7 / 1 * 0.29' as='int((1 + 2)/2) * 7 / 1 * 0.29'
+ pd='2*int((1 + 1)/2) * (7 / 1 + 0.29)' ps='2*int((1 + 2)/2) * (7 / 1 + 0.29)' nrd='0.29 / 7 ' nrs='0.29 / 7 '
+ sa=0 sb=0 sd=0 mult=1 m=1
XM130 VSS VSS VSS VSS sky130_fd_pr__nfet_01v8_lvt L=1 W=7 nf=1 ad='int((1 + 1)/2) * 7 / 1 * 0.29' as='int((1 + 2)/2) * 7 / 1 * 0.29'
+ pd='2*int((1 + 1)/2) * (7 / 1 + 0.29)' ps='2*int((1 + 2)/2) * (7 / 1 + 0.29)' nrd='0.29 / 7 ' nrs='0.29 / 7 '
+ sa=0 sb=0 sd=0 mult=1 m=1
XM131 VSS VSS VSS VSS sky130_fd_pr__nfet_01v8_lvt L=1 W=7 nf=1 ad='int((1 + 1)/2) * 7 / 1 * 0.29' as='int((1 + 2)/2) * 7 / 1 * 0.29'
+ pd='2*int((1 + 1)/2) * (7 / 1 + 0.29)' ps='2*int((1 + 2)/2) * (7 / 1 + 0.29)' nrd='0.29 / 7 ' nrs='0.29 / 7 '
+ sa=0 sb=0 sd=0 mult=1 m=1
XM132 VSS VSS VSS VSS sky130_fd_pr__nfet_01v8_lvt L=1 W=7 nf=1 ad='int((1 + 1)/2) * 7 / 1 * 0.29' as='int((1 + 2)/2) * 7 / 1 * 0.29'
+ pd='2*int((1 + 1)/2) * (7 / 1 + 0.29)' ps='2*int((1 + 2)/2) * (7 / 1 + 0.29)' nrd='0.29 / 7 ' nrs='0.29 / 7 '
+ sa=0 sb=0 sd=0 mult=1 m=1
XM133 VSS VSS VSS VSS sky130_fd_pr__nfet_01v8_lvt L=1 W=7 nf=1 ad='int((1 + 1)/2) * 7 / 1 * 0.29' as='int((1 + 2)/2) * 7 / 1 * 0.29'
+ pd='2*int((1 + 1)/2) * (7 / 1 + 0.29)' ps='2*int((1 + 2)/2) * (7 / 1 + 0.29)' nrd='0.29 / 7 ' nrs='0.29 / 7 '
+ sa=0 sb=0 sd=0 mult=1 m=1
XM134 VSS VSS VSS VSS sky130_fd_pr__nfet_01v8_lvt L=1 W=7 nf=1 ad='int((1 + 1)/2) * 7 / 1 * 0.29' as='int((1 + 2)/2) * 7 / 1 * 0.29'
+ pd='2*int((1 + 1)/2) * (7 / 1 + 0.29)' ps='2*int((1 + 2)/2) * (7 / 1 + 0.29)' nrd='0.29 / 7 ' nrs='0.29 / 7 '
+ sa=0 sb=0 sd=0 mult=1 m=1
XM135 VSS VSS VSS VSS sky130_fd_pr__nfet_01v8_lvt L=1 W=7 nf=1 ad='int((1 + 1)/2) * 7 / 1 * 0.29' as='int((1 + 2)/2) * 7 / 1 * 0.29'
+ pd='2*int((1 + 1)/2) * (7 / 1 + 0.29)' ps='2*int((1 + 2)/2) * (7 / 1 + 0.29)' nrd='0.29 / 7 ' nrs='0.29 / 7 '
+ sa=0 sb=0 sd=0 mult=1 m=1
XM136 VSS VSS VSS VSS sky130_fd_pr__nfet_01v8_lvt L=1 W=7 nf=1 ad='int((1 + 1)/2) * 7 / 1 * 0.29' as='int((1 + 2)/2) * 7 / 1 * 0.29'
+ pd='2*int((1 + 1)/2) * (7 / 1 + 0.29)' ps='2*int((1 + 2)/2) * (7 / 1 + 0.29)' nrd='0.29 / 7 ' nrs='0.29 / 7 '
+ sa=0 sb=0 sd=0 mult=1 m=1
XM137 VSS VSS VSS VSS sky130_fd_pr__nfet_01v8_lvt L=1 W=7 nf=1 ad='int((1 + 1)/2) * 7 / 1 * 0.29' as='int((1 + 2)/2) * 7 / 1 * 0.29'
+ pd='2*int((1 + 1)/2) * (7 / 1 + 0.29)' ps='2*int((1 + 2)/2) * (7 / 1 + 0.29)' nrd='0.29 / 7 ' nrs='0.29 / 7 '
+ sa=0 sb=0 sd=0 mult=1 m=1
XM138 VSS VSS VSS VSS sky130_fd_pr__nfet_01v8_lvt L=1 W=7 nf=1 ad='int((1 + 1)/2) * 7 / 1 * 0.29' as='int((1 + 2)/2) * 7 / 1 * 0.29'
+ pd='2*int((1 + 1)/2) * (7 / 1 + 0.29)' ps='2*int((1 + 2)/2) * (7 / 1 + 0.29)' nrd='0.29 / 7 ' nrs='0.29 / 7 '
+ sa=0 sb=0 sd=0 mult=1 m=1
XM139 VSS VSS VSS VSS sky130_fd_pr__nfet_01v8_lvt L=1 W=7 nf=1 ad='int((1 + 1)/2) * 7 / 1 * 0.29' as='int((1 + 2)/2) * 7 / 1 * 0.29'
+ pd='2*int((1 + 1)/2) * (7 / 1 + 0.29)' ps='2*int((1 + 2)/2) * (7 / 1 + 0.29)' nrd='0.29 / 7 ' nrs='0.29 / 7 '
+ sa=0 sb=0 sd=0 mult=1 m=1
XM140 VSS VSS VSS VSS sky130_fd_pr__nfet_01v8_lvt L=1 W=7 nf=1 ad='int((1 + 1)/2) * 7 / 1 * 0.29' as='int((1 + 2)/2) * 7 / 1 * 0.29'
+ pd='2*int((1 + 1)/2) * (7 / 1 + 0.29)' ps='2*int((1 + 2)/2) * (7 / 1 + 0.29)' nrd='0.29 / 7 ' nrs='0.29 / 7 '
+ sa=0 sb=0 sd=0 mult=1 m=1
XM141 VSS VSS VSS VSS sky130_fd_pr__nfet_01v8_lvt L=1 W=7 nf=1 ad='int((1 + 1)/2) * 7 / 1 * 0.29' as='int((1 + 2)/2) * 7 / 1 * 0.29'
+ pd='2*int((1 + 1)/2) * (7 / 1 + 0.29)' ps='2*int((1 + 2)/2) * (7 / 1 + 0.29)' nrd='0.29 / 7 ' nrs='0.29 / 7 '
+ sa=0 sb=0 sd=0 mult=1 m=1
XM142 VSS VSS VSS VSS sky130_fd_pr__nfet_01v8_lvt L=1 W=7 nf=1 ad='int((1 + 1)/2) * 7 / 1 * 0.29' as='int((1 + 2)/2) * 7 / 1 * 0.29'
+ pd='2*int((1 + 1)/2) * (7 / 1 + 0.29)' ps='2*int((1 + 2)/2) * (7 / 1 + 0.29)' nrd='0.29 / 7 ' nrs='0.29 / 7 '
+ sa=0 sb=0 sd=0 mult=1 m=1
XM143 VSS VSS VSS VSS sky130_fd_pr__nfet_01v8_lvt L=1 W=7 nf=1 ad='int((1 + 1)/2) * 7 / 1 * 0.29' as='int((1 + 2)/2) * 7 / 1 * 0.29'
+ pd='2*int((1 + 1)/2) * (7 / 1 + 0.29)' ps='2*int((1 + 2)/2) * (7 / 1 + 0.29)' nrd='0.29 / 7 ' nrs='0.29 / 7 '
+ sa=0 sb=0 sd=0 mult=1 m=1
XM144 VSS VSS VSS VSS sky130_fd_pr__nfet_01v8_lvt L=1 W=7 nf=1 ad='int((1 + 1)/2) * 7 / 1 * 0.29' as='int((1 + 2)/2) * 7 / 1 * 0.29'
+ pd='2*int((1 + 1)/2) * (7 / 1 + 0.29)' ps='2*int((1 + 2)/2) * (7 / 1 + 0.29)' nrd='0.29 / 7 ' nrs='0.29 / 7 '
+ sa=0 sb=0 sd=0 mult=1 m=1
XM145 VSS VSS VSS VSS sky130_fd_pr__nfet_01v8_lvt L=1 W=7 nf=1 ad='int((1 + 1)/2) * 7 / 1 * 0.29' as='int((1 + 2)/2) * 7 / 1 * 0.29'
+ pd='2*int((1 + 1)/2) * (7 / 1 + 0.29)' ps='2*int((1 + 2)/2) * (7 / 1 + 0.29)' nrd='0.29 / 7 ' nrs='0.29 / 7 '
+ sa=0 sb=0 sd=0 mult=1 m=1
XR1 net1 Vout1 VSS sky130_fd_pr__res_xhigh_po_1p41 L=14 mult=1 m=1
.ends

.GLOBAL GND
.end
